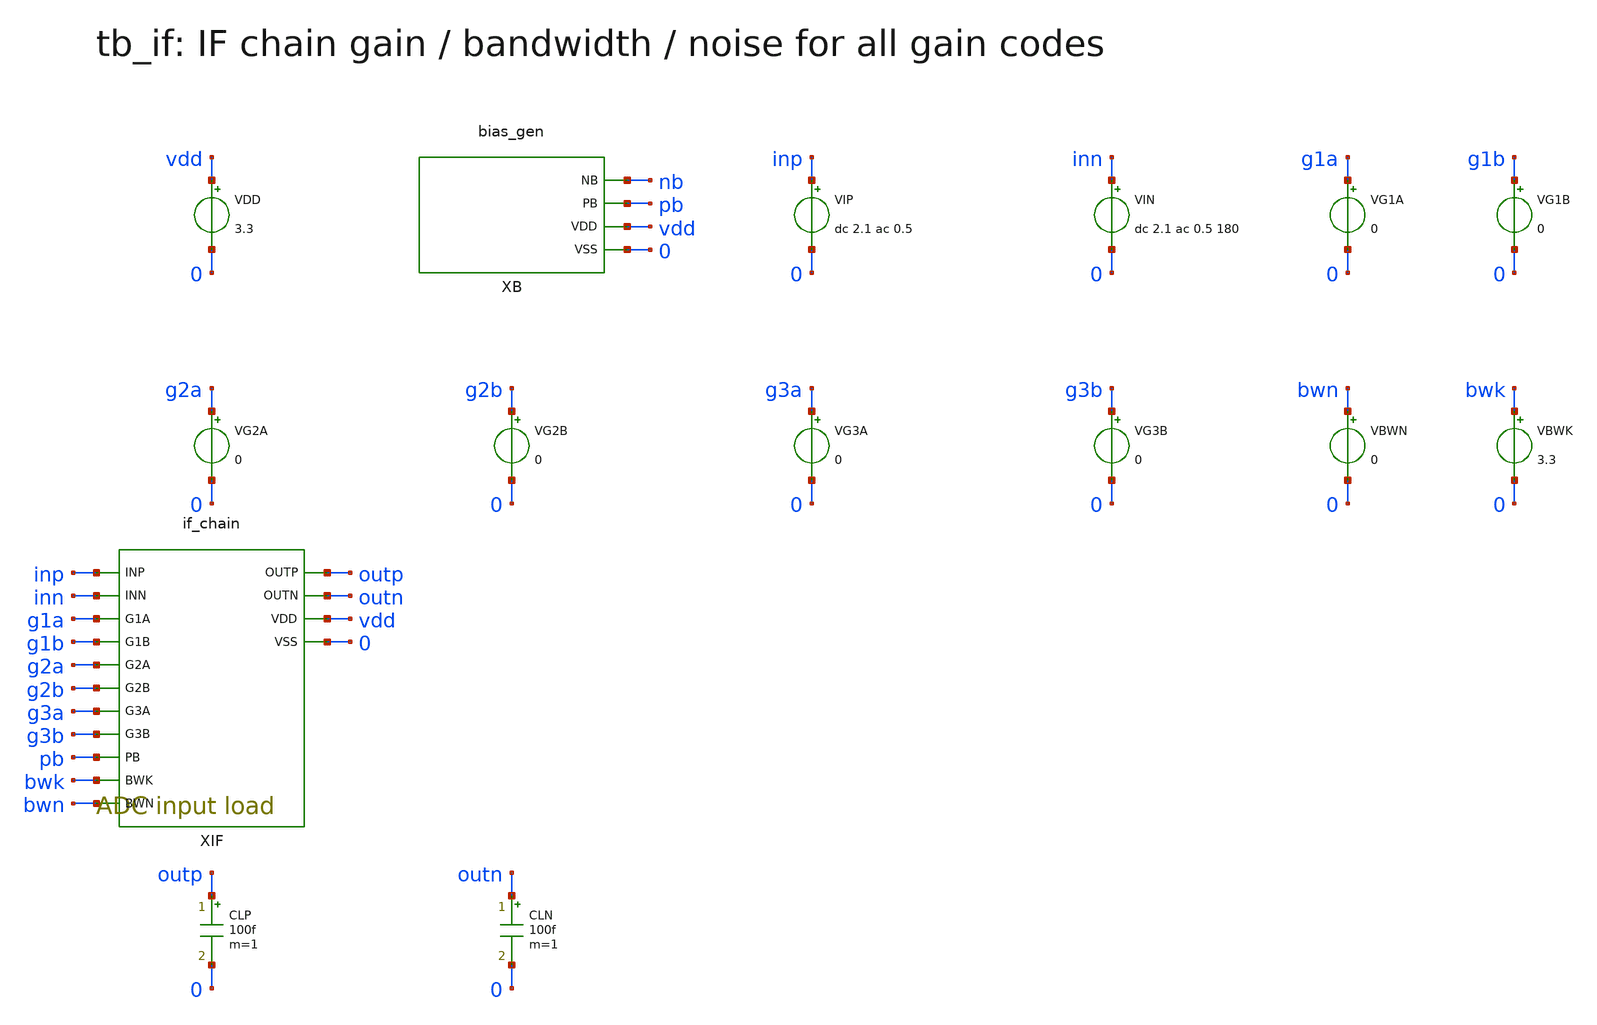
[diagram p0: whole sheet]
** sch_path: v1_claude/xschem/tb_if.sch
**.subckt tb_if
VDD vdd 0 3.3
XB nb pb vdd 0 bias_gen
VIP inp 0 dc 2.1 ac 0.5
VIN inn 0 dc 2.1 ac 0.5 180
VG1A g1a 0 0
VG1B g1b 0 0
VG2A g2a 0 0
VG2B g2b 0 0
VG3A g3a 0 0
VG3B g3b 0 0
VBWN bwn 0 0
VBWK bwk 0 3.3
XIF inp inn g1a g1b g2a g2b g3a g3b pb bwk bwn outp outn vdd 0 if_chain
CLP outp 0 100f m=1
CLN outn 0 100f m=1
**** begin user architecture code
 .include $::180MCU_MODELS/design.ngspice
.lib $::180MCU_MODELS/sm141064.ngspice typical
.lib $::180MCU_MODELS/sm141064.ngspice res_typical
.lib $::180MCU_MODELS/sm141064.ngspice mimcap_typical

.control
set num_threads=1
op
echo RES op nbif=$&v(xif.nbif) pbif=$&v(xif.pbif) ix=$&v(xif.xbif.x) vdiv=$&v(xif.xbif.vdiv)
+ a1p=$&v(xif.a1p) f1p=$&v(xif.f1p) a2p=$&v(xif.a2p) f2p=$&v(xif.f2p) outp=$&v(outp)
alter VG1A dc = 0
alter VG1B dc = 0
alter VG2A dc = 0
alter VG2B dc = 0
alter VG3A dc = 0
alter VG3B dc = 0
ac dec 40 1e4 1e9
let g = db(v(outp)-v(outn))
meas ac g4 find g at=4.092e6
meas ac g66 find g at=6.6e6
meas ac g112 find g at=11.25e6
meas ac g164 find g at=16.368e6
meas ac gmax max g
let gm3 = gmax - 3
meas ac fl when g=gm3 rise=1
meas ac fh when g=gm3 fall=last
echo RES code=0 g4=$&g4 g6.6=$&g66 g11.25=$&g112 g16.4=$&g164 gmax=$&gmax fl=$&fl fh=$&fh
wrdata if_ac_code0 g
noise v(outp,outn) VIP dec 20 1e5 1e8
setplot noise1
wrdata if_noise_code0 inoise_spectrum onoise_spectrum
alter VG1A dc = 3.3
alter VG1B dc = 0
alter VG2A dc = 3.3
alter VG2B dc = 0
alter VG3A dc = 3.3
alter VG3B dc = 0
ac dec 40 1e4 1e9
let g = db(v(outp)-v(outn))
meas ac g4 find g at=4.092e6
meas ac g66 find g at=6.6e6
meas ac g112 find g at=11.25e6
meas ac g164 find g at=16.368e6
meas ac gmax max g
let gm3 = gmax - 3
meas ac fl when g=gm3 rise=1
meas ac fh when g=gm3 fall=last
echo RES code=1 g4=$&g4 g6.6=$&g66 g11.25=$&g112 g16.4=$&g164 gmax=$&gmax fl=$&fl fh=$&fh
wrdata if_ac_code1 g
noise v(outp,outn) VIP dec 20 1e5 1e8
setplot noise3
wrdata if_noise_code1 inoise_spectrum onoise_spectrum
alter VG1A dc = 0
alter VG1B dc = 3.3
alter VG2A dc = 0
alter VG2B dc = 3.3
alter VG3A dc = 0
alter VG3B dc = 3.3
ac dec 40 1e4 1e9
let g = db(v(outp)-v(outn))
meas ac g4 find g at=4.092e6
meas ac g66 find g at=6.6e6
meas ac g112 find g at=11.25e6
meas ac g164 find g at=16.368e6
meas ac gmax max g
let gm3 = gmax - 3
meas ac fl when g=gm3 rise=1
meas ac fh when g=gm3 fall=last
echo RES code=2 g4=$&g4 g6.6=$&g66 g11.25=$&g112 g16.4=$&g164 gmax=$&gmax fl=$&fl fh=$&fh
wrdata if_ac_code2 g
noise v(outp,outn) VIP dec 20 1e5 1e8
setplot noise5
wrdata if_noise_code2 inoise_spectrum onoise_spectrum
alter VG1A dc = 3.3
alter VG1B dc = 3.3
alter VG2A dc = 3.3
alter VG2B dc = 3.3
alter VG3A dc = 3.3
alter VG3B dc = 3.3
ac dec 40 1e4 1e9
let g = db(v(outp)-v(outn))
meas ac g4 find g at=4.092e6
meas ac g66 find g at=6.6e6
meas ac g112 find g at=11.25e6
meas ac g164 find g at=16.368e6
meas ac gmax max g
let gm3 = gmax - 3
meas ac fl when g=gm3 rise=1
meas ac fh when g=gm3 fall=last
echo RES code=3 g4=$&g4 g6.6=$&g66 g11.25=$&g112 g16.4=$&g164 gmax=$&gmax fl=$&fl fh=$&fh
wrdata if_ac_code3 g
noise v(outp,outn) VIP dec 20 1e5 1e8
setplot noise7
wrdata if_noise_code3 inoise_spectrum onoise_spectrum
.endc

**** end user architecture code
**.ends
.end
